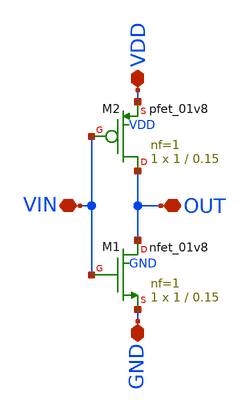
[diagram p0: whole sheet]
** sch_path: Inverter project/untitled-1.sch
**.subckt untitled-1 OUT VIN VDD GND
*.iopin OUT
*.iopin VIN
*.iopin VDD
*.iopin GND
XM1 OUT VIN GND GND sky130_fd_pr__nfet_01v8 L=0.15 W=1 nf=1 ad='int((nf+1)/2) * W/nf * 0.29' as='int((nf+2)/2) * W/nf * 0.29'
+ pd='2*int((nf+1)/2) * (W/nf + 0.29)' ps='2*int((nf+2)/2) * (W/nf + 0.29)' nrd='0.29 / W' nrs='0.29 / W'
+ sa=0 sb=0 sd=0 mult=1 m=1
XM2 OUT VIN VDD VDD sky130_fd_pr__pfet_01v8 L=0.15 W=1 nf=1 ad='int((nf+1)/2) * W/nf * 0.29' as='int((nf+2)/2) * W/nf * 0.29'
+ pd='2*int((nf+1)/2) * (W/nf + 0.29)' ps='2*int((nf+2)/2) * (W/nf + 0.29)' nrd='0.29 / W' nrs='0.29 / W'
+ sa=0 sb=0 sd=0 mult=1 m=1
**.ends
.end
